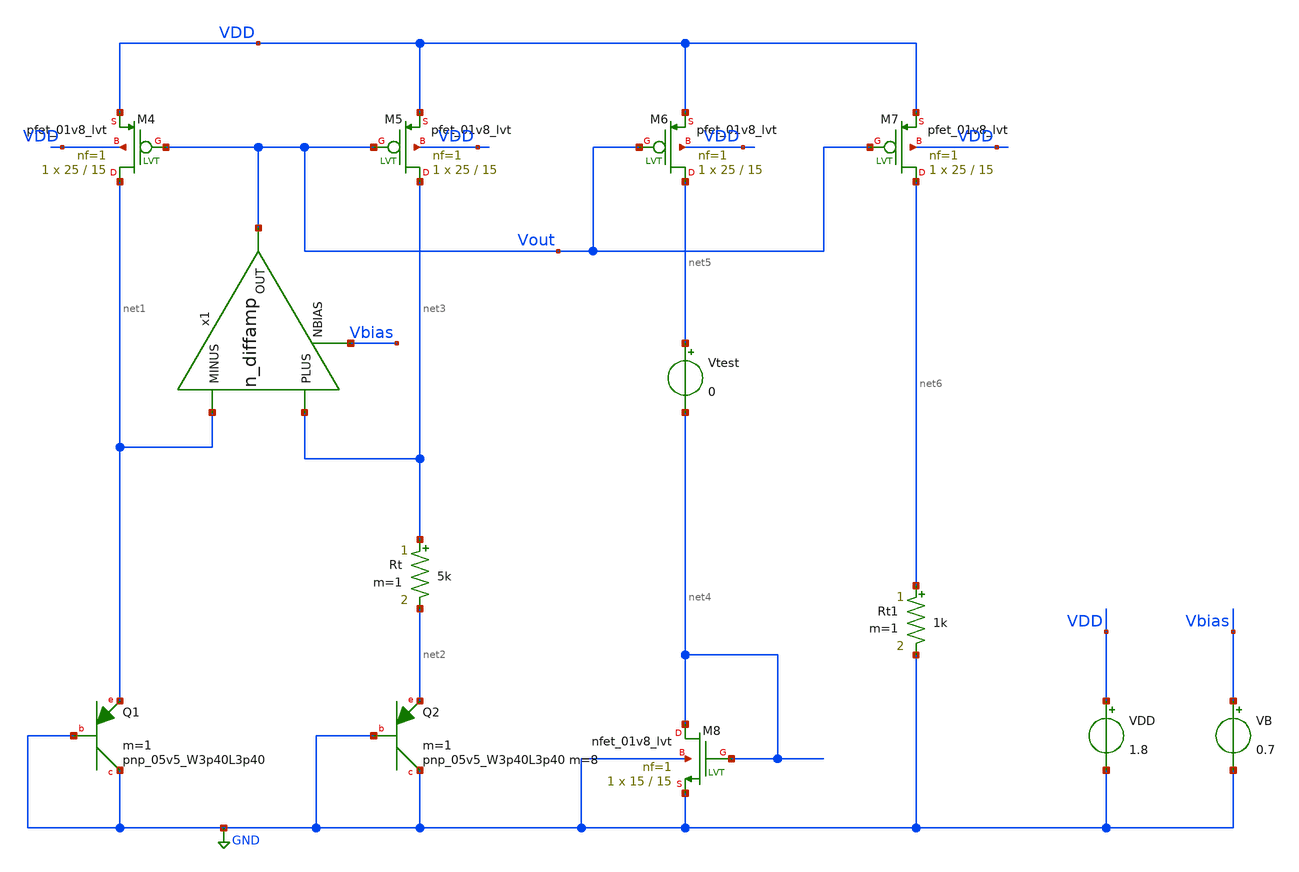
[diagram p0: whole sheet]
** sch_path: design/bgr_new/BGR_nocas.sch
* Copyright 2021 Stefan Frederik Schippers
* Licensed under the Apache License, Version 2.0 (the "License");
* you may not use this file except in compliance with the License.
* You may obtain a copy of the License at
* https://www.apache.org/licenses/LICENSE-2.0
* Unless required by applicable law or agreed to in writing, software
* distributed under the License is distributed on an "AS IS" BASIS,
* WITHOUT WARRANTIES OR CONDITIONS OF ANY KIND, either express or implied.
* See the License for the specific language governing permissions and
* limitations under the License.
**.subckt BGR_nocas
XQ1 GND GND net1 sky130_fd_pr__pnp_05v5_W3p40L3p40 m=1
XQ2 GND GND net2 sky130_fd_pr__pnp_05v5_W3p40L3p40 m=8 m=1
XM4 net1 Vout VDD VDD sky130_fd_pr__pfet_01v8_lvt L=15 W=25 nf=1 ad='int((nf+1)/2) * W * 0.29' as='int((nf+2)/2) * W * 0.29'
+ pd='2*int((nf+1)/2) * (W + 0.29)' ps='2*int((nf+2)/2) * (W + 0.29)' nrd='0.29 / W / nf' nrs='0.29 / W / nf'
+ sa=0 sb=0 sd=0 mult=1 m=1
XM5 net3 Vout VDD VDD sky130_fd_pr__pfet_01v8_lvt L=15 W=25 nf=1 ad='int((nf+1)/2) * W * 0.29' as='int((nf+2)/2) * W * 0.29'
+ pd='2*int((nf+1)/2) * (W + 0.29)' ps='2*int((nf+2)/2) * (W + 0.29)' nrd='0.29 / W / nf' nrs='0.29 / W / nf'
+ sa=0 sb=0 sd=0 mult=1 m=1
XM6 net5 Vout VDD VDD sky130_fd_pr__pfet_01v8_lvt L=15 W=25 nf=1 ad='int((nf+1)/2) * W * 0.29' as='int((nf+2)/2) * W * 0.29'
+ pd='2*int((nf+1)/2) * (W + 0.29)' ps='2*int((nf+2)/2) * (W + 0.29)' nrd='0.29 / W / nf' nrs='0.29 / W / nf'
+ sa=0 sb=0 sd=0 mult=1 m=1
XM7 net6 Vout VDD VDD sky130_fd_pr__pfet_01v8_lvt L=15 W=25 nf=1 ad='int((nf+1)/2) * W * 0.29' as='int((nf+2)/2) * W * 0.29'
+ pd='2*int((nf+1)/2) * (W + 0.29)' ps='2*int((nf+2)/2) * (W + 0.29)' nrd='0.29 / W / nf' nrs='0.29 / W / nf'
+ sa=0 sb=0 sd=0 mult=1 m=1
XM8 net4 net4 GND GND sky130_fd_pr__nfet_01v8_lvt L=15 W=15 nf=1 ad='int((nf+1)/2) * W/nf * 0.29' as='int((nf+2)/2) * W/nf * 0.29'
+ pd='2*int((nf+1)/2) * (W/nf + 0.29)' ps='2*int((nf+2)/2) * (W/nf + 0.29)' nrd='0.29 / W' nrs='0.29 / W'
+ sa=0 sb=0 sd=0 mult=1 m=1
Vtest net5 net4 0
Rt1 net6 GND 1k m=1
Rt net3 net2 5k m=1
VDD VDD GND 1.8
x1 Vout net1 net3 Vbias n_diffamp
VB Vbias GND 0.7
**** begin user architecture code

** opencircuitdesign pdks install
.lib $::SKYWATER_MODELS/sky130.lib.spice tt_mm




.options savecurrents

*** plot vbgp with variation in supply voltage
*Vdd VDD GND 3.3
*V_en en GND 3.3
*.dc Vdd 2 4 0.1
*.control
*run
*print Vbgp
*plot V(Vbgp)
*.endc

*** plot vbgp with variation in temperature @3.3V
*Vdd VDD GND 3.3
*V_en en GND 3.3
.dc temp -40 100 1 Rt 5k 8k 0.2k
*.dc temp -40 100 1

.control
run
*print V(VE)
*plot V(VE)
*plot deriv(V(VE))/1.202344
plot V(Vout)
plot deriv(V(Vout))/1.202344
.endc

*** plot voltage coefficient
*Vdd VDD GND 3.3
*V_en en GND 3.3
*.dc Vdd 2 4 0.1
*.control
*run
*plot deriv(V(Vbgp))
*.endc

*** plot temperature coefficient
*Vdd VDD GND 3.3
*V_en en GND 3.3
*.dc temp -40 140 1
*.control
*run
*plot deriv(V(Vbgp))/1.202344
*.endc



*** enable pin
*Vdd VDD GND 3.3
*V_en en GND PULSE(0 3.3 0 200us 200us 600us 2000us 0)
*.tran 1u 2000us
*.control
*run
*plot V(en)
*plot -I(VDD)
*.endc


**** end user architecture code
**.ends

* expanding   symbol:  sky130_tests/n_diffamp.sym # of pins=4
** sym_path: sky130_tests/n_diffamp.sym
** sch_path: sky130_tests/n_diffamp.sch
.subckt n_diffamp OUT MINUS PLUS NBIAS
*.ipin PLUS
*.ipin MINUS
*.opin OUT
*.ipin NBIAS
XM1 net1 PLUS S GND sky130_fd_pr__nfet_01v8_lvt L=0.3 W=2 nf=1 ad='int((1 + 1)/2) * 2 / 1 * 0.29' as='int((1 + 2)/2) * 2 / 1 * 0.29'
+ pd='2*int((1 + 1)/2) * (2 / 1 + 0.29)' ps='2*int((1 + 2)/2) * (2 / 1 + 0.29)' nrd='0.29 / 2 ' nrs='0.29 / 2 '
+ sa=0 sb=0 sd=0 mult=1 m=1
XM2 OUT MINUS S GND sky130_fd_pr__nfet_01v8_lvt L=0.3 W=2 nf=1 ad='int((1 + 1)/2) * 2 / 1 * 0.29' as='int((1 + 2)/2) * 2 / 1 * 0.29'
+ pd='2*int((1 + 1)/2) * (2 / 1 + 0.29)' ps='2*int((1 + 2)/2) * (2 / 1 + 0.29)' nrd='0.29 / 2 ' nrs='0.29 / 2 '
+ sa=0 sb=0 sd=0 mult=1 m=1
XM3 OUT net1 VDD VDD sky130_fd_pr__pfet_01v8_lvt L=0.8 W=4 nf=1 ad='int((1 + 1)/2) * 4 / 1 * 0.29' as='int((1 + 2)/2) * 4 / 1 * 0.29'
+ pd='2*int((1 + 1)/2) * (4 / 1 + 0.29)' ps='2*int((1 + 2)/2) * (4 / 1 + 0.29)' nrd='0.29 / 4 ' nrs='0.29 / 4 '
+ sa=0 sb=0 sd=0 mult=1 m=1
XM4 net1 net1 VDD VDD sky130_fd_pr__pfet_01v8_lvt L=0.8 W=4 nf=1 ad='int((1 + 1)/2) * 4 / 1 * 0.29' as='int((1 + 2)/2) * 4 / 1 * 0.29'
+ pd='2*int((1 + 1)/2) * (4 / 1 + 0.29)' ps='2*int((1 + 2)/2) * (4 / 1 + 0.29)' nrd='0.29 / 4 ' nrs='0.29 / 4 '
+ sa=0 sb=0 sd=0 mult=1 m=1
XM5 net2 NBIAS GND GND sky130_fd_pr__nfet_01v8 L=2 W=0.7 nf=1 ad='int((nf+1)/2) * W/nf * 0.29' as='int((nf+2)/2) * W/nf * 0.29'
+ pd='2*int((nf+1)/2) * (W/nf + 0.29)' ps='2*int((nf+2)/2) * (W/nf + 0.29)' nrd='0.29 / W' nrs='0.29 / W'
+ sa=0 sb=0 sd=0 mult=1 m=1
XR1 GND S GND sky130_fd_pr__res_xhigh_po_0p35 L=50 mult=1 m=1
V5 S net2 0
.save i(v5)
.ends

.GLOBAL GND
.GLOBAL VDD
.end
